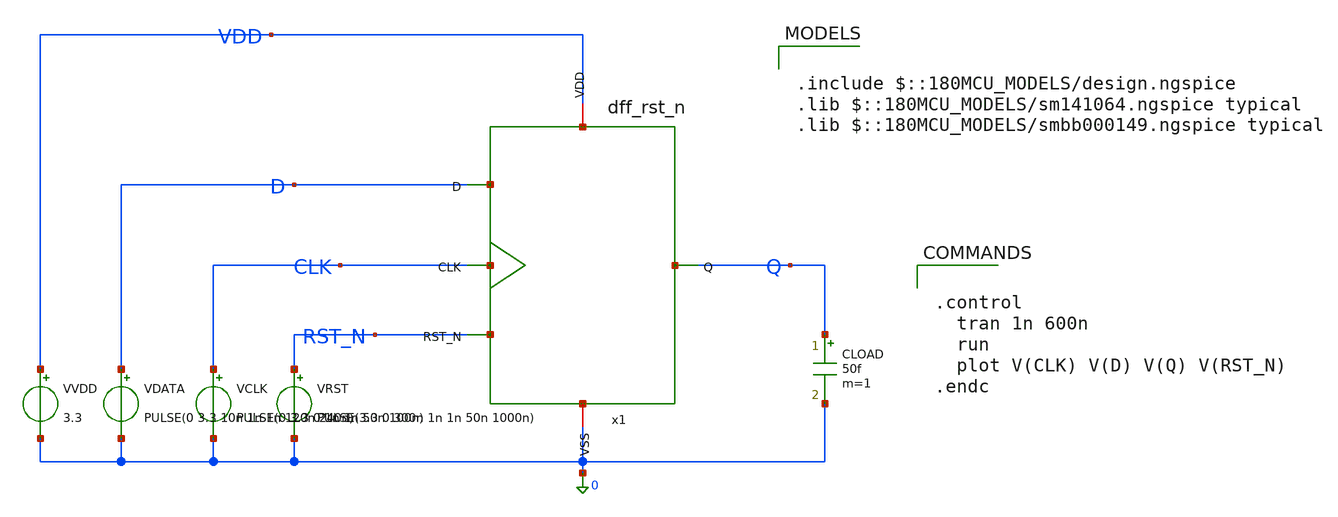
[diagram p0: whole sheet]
** sch_path: sar_logic/sar_designs/tb_dff_rst_n.sch
**.subckt tb_dff_rst_n
x1 VDD CLK D Q RST_N 0 dff_rst_n
VRST RST_N 0 PULSE(3.3 0 300n 1n 1n 50n 1000n)
VCLK CLK 0 PULSE(0 3.3 0 1n 1n 50n 100n)
VDATA D 0 PULSE(0 3.3 10n 1n 1n 120n 240n)
VVDD VDD 0 3.3
CLOAD Q 0 50f m=1
**** begin user architecture code

.include $::180MCU_MODELS/design.ngspice
.lib $::180MCU_MODELS/sm141064.ngspice typical
.lib $::180MCU_MODELS/smbb000149.ngspice typical



.control
  tran 1n 600n
  run
  plot V(CLK) V(D) V(Q) V(RST_N)
.endc


**** end user architecture code
**.ends

* expanding   symbol:  dff_rst_n.sym # of pins=6
** sym_path: sar_logic/sar_designs/dff_rst_n.sym
** sch_path: sar_logic/sar_designs/dff_rst_n.sch
.subckt dff_rst_n VDD CLK D Q RST_N VSS
*.ipin D
*.ipin CLK
*.ipin RST_N
*.opin Q
*.iopin VDD
*.iopin VSS
x1 CLK VSS net4 net1 VDD net7 tg
x2 net7 VSS D net1 VDD CLK tg
x3 CLK VSS net4 net2 VDD net7 tg
x4 net7 VSS net6 net2 VDD CLK tg
x5 VDD net3 net1 RST_N VSS nand2
x6 VDD net5 net2 RST_N VSS nand2
x7 VDD net3 net4 VSS inv
x8 VDD net5 Q VSS inv
x9 VDD net5 net6 VSS inv
x10 VDD CLK net7 VSS inv
.ends


* expanding   symbol:  tg.sym # of pins=6
** sym_path: sar_logic/sar_designs/tg.sym
** sch_path: sar_logic/sar_designs/tg.sch
.subckt tg CTRL VSS A B VDD CTRL_B
*.iopin VDD
*.iopin VSS
*.iopin A
*.iopin B
*.ipin CTRL_B
*.ipin CTRL
XM1 A CTRL_B B VDD pfet_03v3 L=0.28u W=1u nf=1 ad='int((nf+1)/2) * W/nf * 0.18u' as='int((nf+2)/2) * W/nf * 0.18u'
+ pd='2*int((nf+1)/2) * (W/nf + 0.18u)' ps='2*int((nf+2)/2) * (W/nf + 0.18u)' nrd='0.18u / W' nrs='0.18u / W'
+ sa=0 sb=0 sd=0 m=1
XM2 A CTRL B VSS nfet_03v3 L=0.28u W=0.5u nf=1 ad='int((nf+1)/2) * W/nf * 0.18u' as='int((nf+2)/2) * W/nf * 0.18u'
+ pd='2*int((nf+1)/2) * (W/nf + 0.18u)' ps='2*int((nf+2)/2) * (W/nf + 0.18u)' nrd='0.18u / W' nrs='0.18u / W'
+ sa=0 sb=0 sd=0 m=1
.ends


* expanding   symbol:  nand2.sym # of pins=5
** sym_path: sar_logic/sar_designs/nand2.sym
** sch_path: sar_logic/sar_designs/nand2.sch
.subckt nand2 VDD Z A B VSS
*.ipin A
*.ipin B
*.iopin VSS
*.iopin VDD
*.opin Z
XM1 Z A VDD VDD pfet_03v3 L=0.28u W=1u nf=1 ad='int((nf+1)/2) * W/nf * 0.18u' as='int((nf+2)/2) * W/nf * 0.18u'
+ pd='2*int((nf+1)/2) * (W/nf + 0.18u)' ps='2*int((nf+2)/2) * (W/nf + 0.18u)' nrd='0.18u / W' nrs='0.18u / W'
+ sa=0 sb=0 sd=0 m=1
XM2 Z B VDD VDD pfet_03v3 L=0.28u W=1u nf=1 ad='int((nf+1)/2) * W/nf * 0.18u' as='int((nf+2)/2) * W/nf * 0.18u'
+ pd='2*int((nf+1)/2) * (W/nf + 0.18u)' ps='2*int((nf+2)/2) * (W/nf + 0.18u)' nrd='0.18u / W' nrs='0.18u / W'
+ sa=0 sb=0 sd=0 m=1
XM3 Z A net1 VSS nfet_03v3 L=0.28u W=1u nf=1 ad='int((nf+1)/2) * W/nf * 0.18u' as='int((nf+2)/2) * W/nf * 0.18u'
+ pd='2*int((nf+1)/2) * (W/nf + 0.18u)' ps='2*int((nf+2)/2) * (W/nf + 0.18u)' nrd='0.18u / W' nrs='0.18u / W'
+ sa=0 sb=0 sd=0 m=1
XM4 net1 B VSS VSS nfet_03v3 L=0.28u W=1u nf=1 ad='int((nf+1)/2) * W/nf * 0.18u' as='int((nf+2)/2) * W/nf * 0.18u'
+ pd='2*int((nf+1)/2) * (W/nf + 0.18u)' ps='2*int((nf+2)/2) * (W/nf + 0.18u)' nrd='0.18u / W' nrs='0.18u / W'
+ sa=0 sb=0 sd=0 m=1
.ends


* expanding   symbol:  inv.sym # of pins=4
** sym_path: sar_logic/sar_designs/inv.sym
** sch_path: sar_logic/sar_designs/inv.sch
.subckt inv VDD vin vout VSS
*.ipin vin
*.opin vout
*.iopin VDD
*.iopin VSS
XM1 vout vin VDD VDD pfet_03v3 L=0.28u W=1u nf=1 ad='int((nf+1)/2) * W/nf * 0.18u' as='int((nf+2)/2) * W/nf * 0.18u'
+ pd='2*int((nf+1)/2) * (W/nf + 0.18u)' ps='2*int((nf+2)/2) * (W/nf + 0.18u)' nrd='0.18u / W' nrs='0.18u / W'
+ sa=0 sb=0 sd=0 m=1
XM2 vout vin VSS VSS nfet_03v3 L=0.28u W=0.5u nf=1 ad='int((nf+1)/2) * W/nf * 0.18u' as='int((nf+2)/2) * W/nf * 0.18u'
+ pd='2*int((nf+1)/2) * (W/nf + 0.18u)' ps='2*int((nf+2)/2) * (W/nf + 0.18u)' nrd='0.18u / W' nrs='0.18u / W'
+ sa=0 sb=0 sd=0 m=1
.ends

.end
